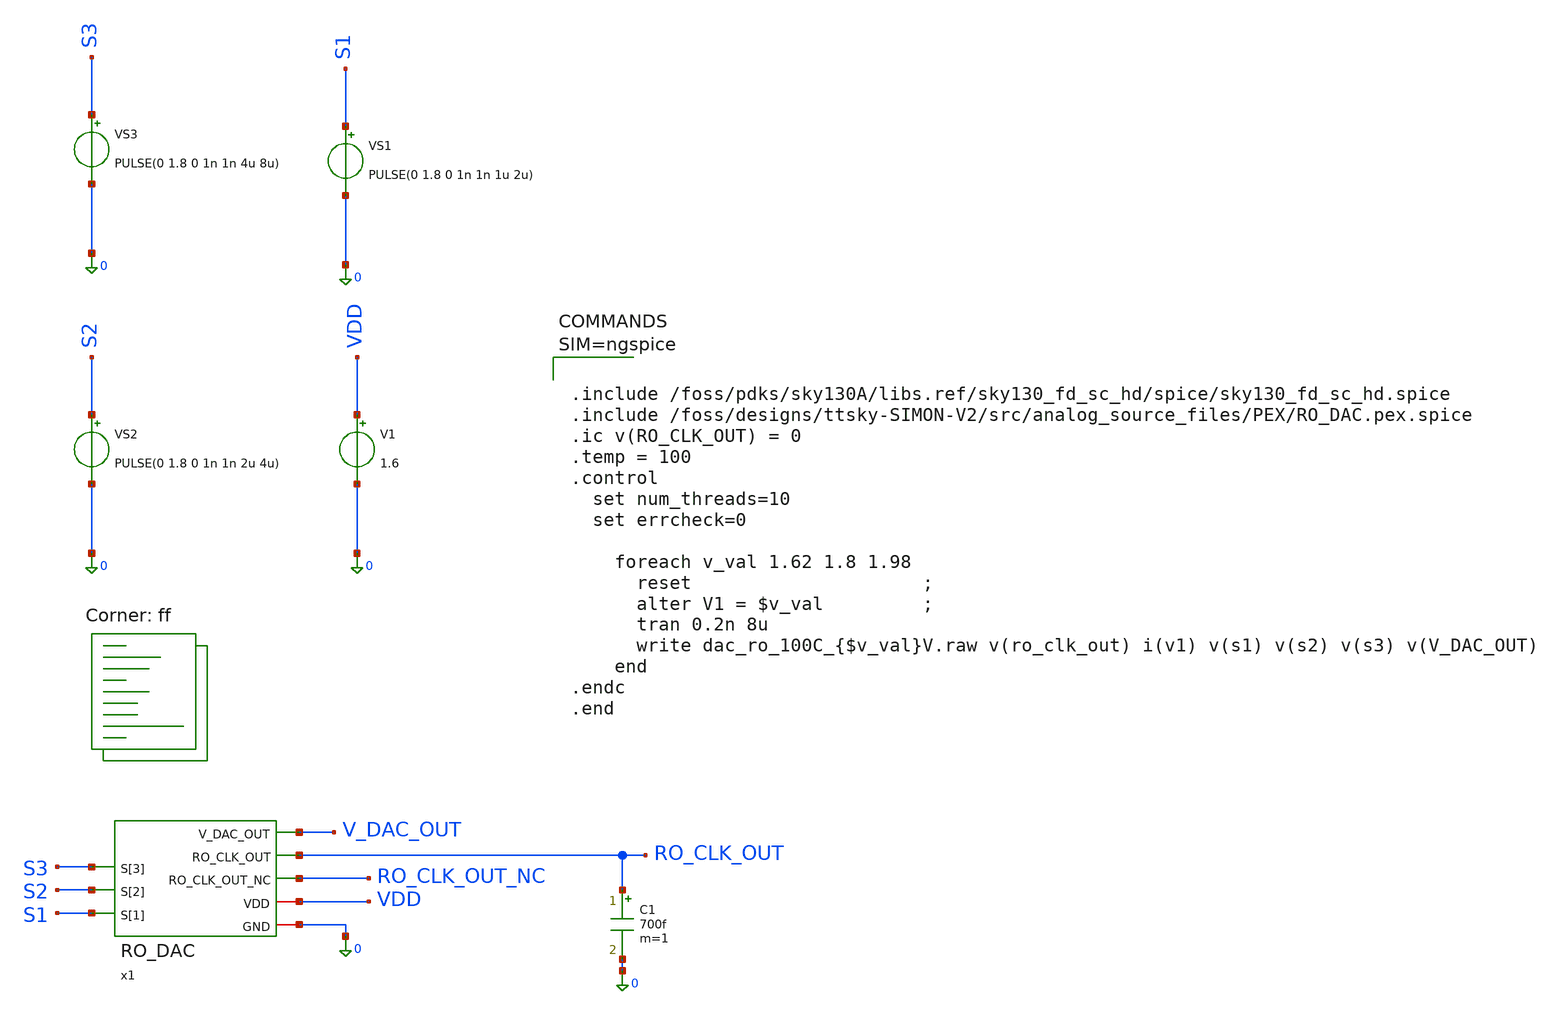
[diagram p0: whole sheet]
** sch_path: src/analog_source_files/RO_DAC_tb.sch
**.subckt RO_DAC_tb
x1 RO_CLK_OUT S3 RO_CLK_OUT_NC S2 S1 VDD 0 V_DAC_OUT RO_DAC
V1 VDD 0 1.6
VS1 S1 0 PULSE(0 1.8 0 1n 1n 1u 2u)
VS2 S2 0 PULSE(0 1.8 0 1n 1n 2u 4u)
VS3 S3 0 PULSE(0 1.8 0 1n 1n 4u 8u)
C1 RO_CLK_OUT 0 700f m=1
**** begin user architecture code
.lib $::SKYWATER_MODELS/sky130.lib.spice ff



.include /foss/pdks/sky130A/libs.ref/sky130_fd_sc_hd/spice/sky130_fd_sc_hd.spice
.include /foss/designs/ttsky-SIMON-V2/src/analog_source_files/PEX/RO_DAC.pex.spice
.ic v(RO_CLK_OUT) = 0
.temp = 100
.control
  set num_threads=10
  set errcheck=0

    foreach v_val 1.62 1.8 1.98
      reset                     ;
      alter V1 = $v_val         ;
      tran 0.2n 8u
      write dac_ro_100C_{$v_val}V.raw v(ro_clk_out) i(v1) v(s1) v(s2) v(s3) v(V_DAC_OUT)
    end
.endc
.end



**** end user architecture code
**.ends
.end
